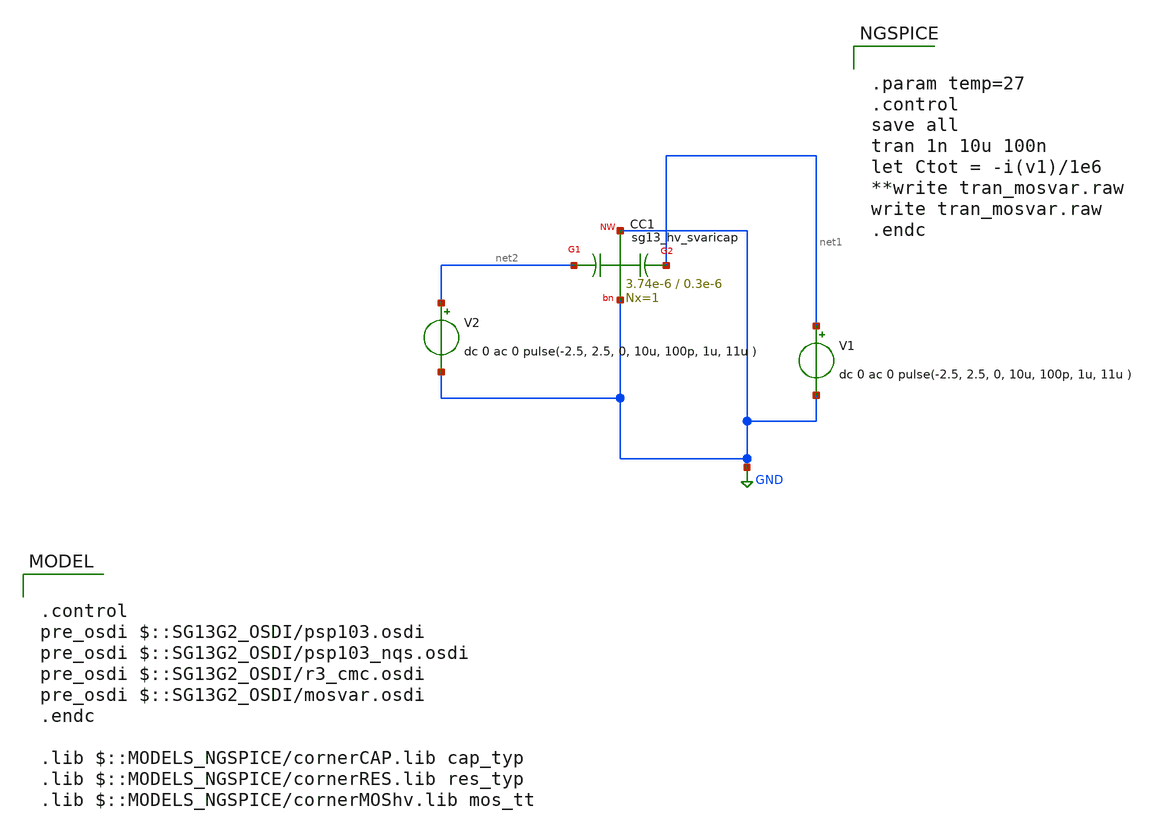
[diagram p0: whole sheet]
** sch_path: ihp-sg13g2/xschem_libs/sg13g2_tests/tran_svaricap_test/schematic/tran_svaricap_test.sch
**.subckt tran_svaricap_test
XC1 net2 GND net1 GND sg13_hv_svaricap w=3.74e-6 l=0.3e-6 Nx=1
V1 net1 GND dc 0 ac 0 pulse(-2.5, 2.5, 0, 10u, 100p, 1u, 11u )
V2 net2 GND dc 0 ac 0 pulse(-2.5, 2.5, 0, 10u, 100p, 1u, 11u )
**** begin user architecture code

.control
pre_osdi $::SG13G2_OSDI/psp103.osdi
pre_osdi $::SG13G2_OSDI/psp103_nqs.osdi
pre_osdi $::SG13G2_OSDI/r3_cmc.osdi
pre_osdi $::SG13G2_OSDI/mosvar.osdi
.endc

.lib $::MODELS_NGSPICE/cornerCAP.lib cap_typ
.lib $::MODELS_NGSPICE/cornerRES.lib res_typ
.lib $::MODELS_NGSPICE/cornerMOShv.lib mos_tt



.param temp=27
.control
save all
tran 1n 10u 100n
let Ctot = -i(v1)/1e6
**write tran_mosvar.raw
write tran_mosvar.raw
.endc


**** end user architecture code
**.ends
.GLOBAL GND
.end
